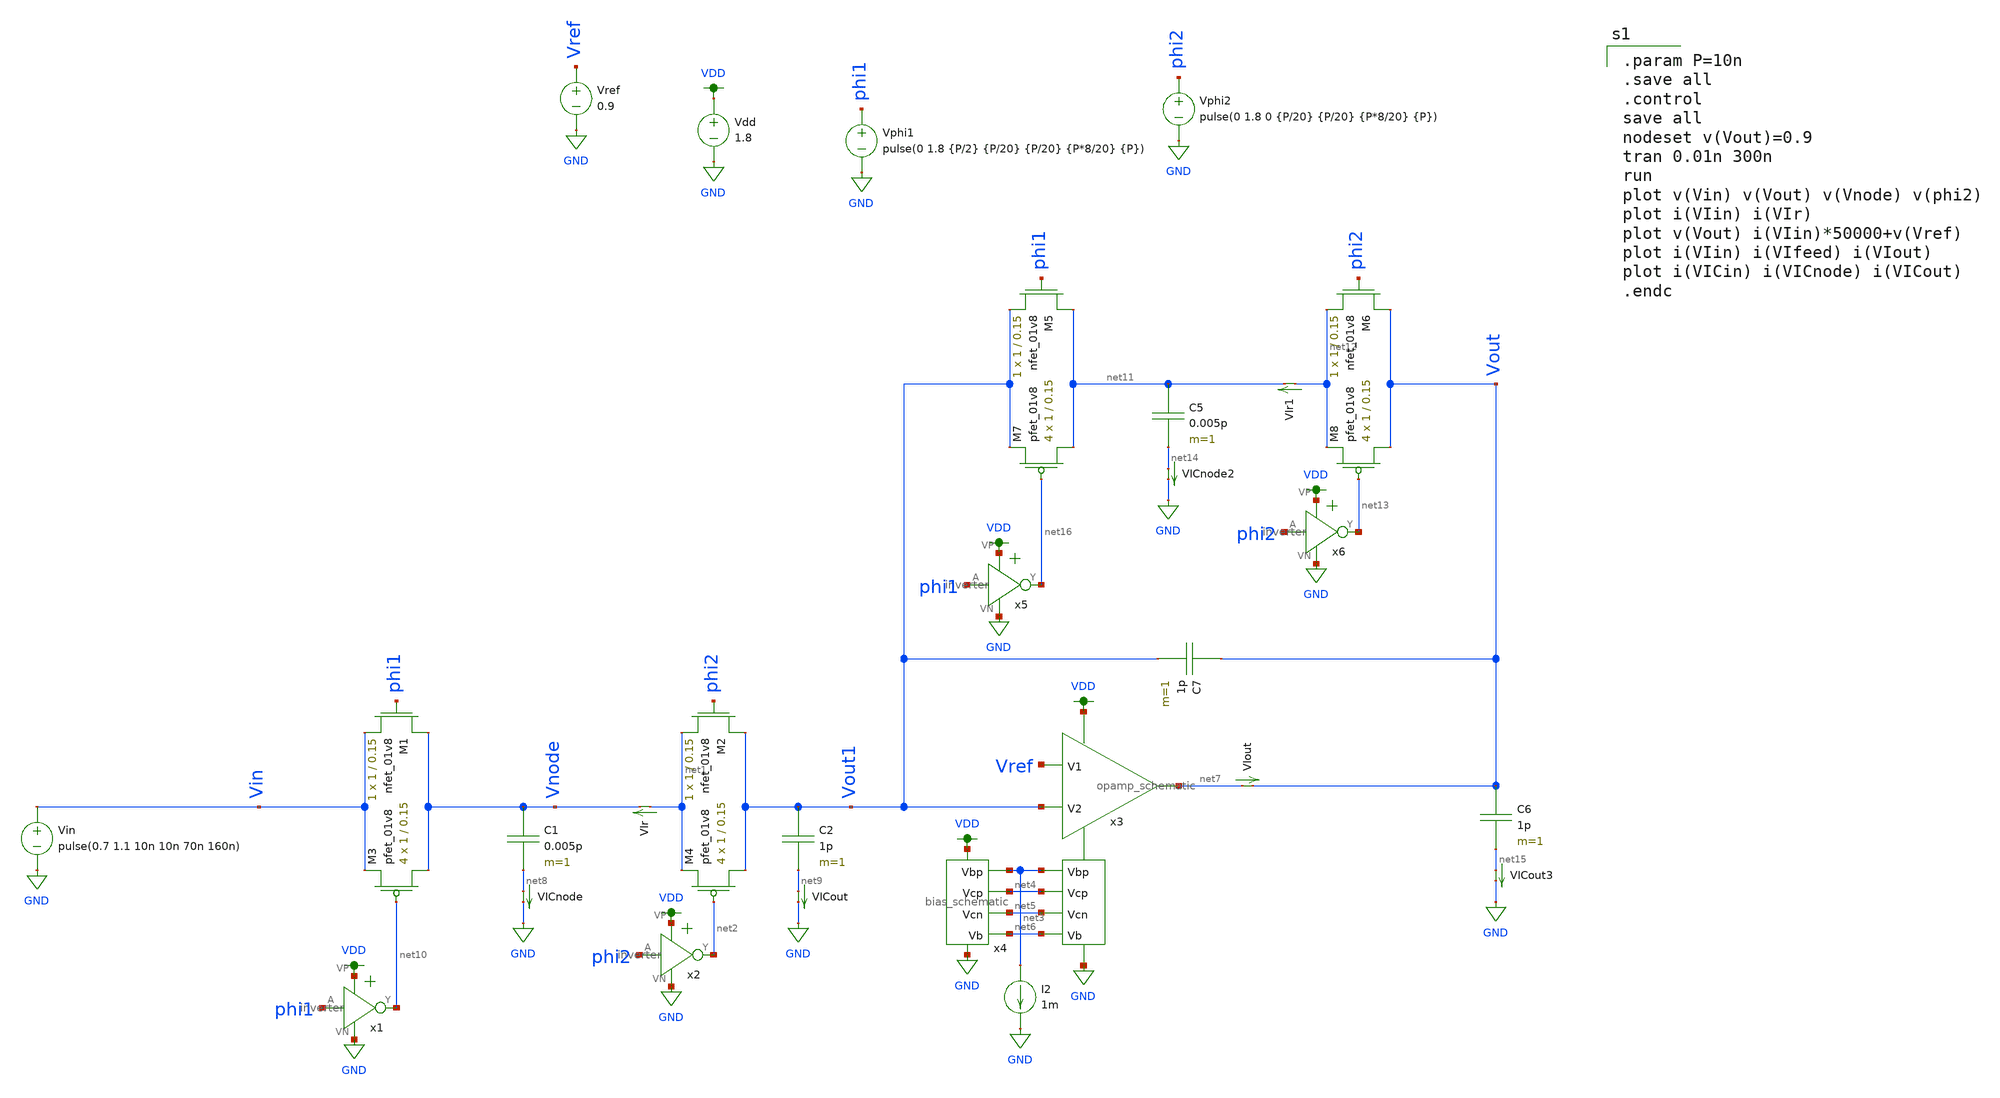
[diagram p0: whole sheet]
** sch_path: xschem/switched_capacitor/switched_capacitor_second_stage_lpf.sch
**.subckt switched_capacitor_second_stage_lpf
C1 Vnode net8 0.005p m=1
XM1 Vnode phi1 Vin GND sky130_fd_pr__nfet_01v8 L=0.15 W=1 nf=1 ad='int((nf+1)/2) * W/nf * 0.29' as='int((nf+2)/2) * W/nf * 0.29'
+ pd='2*int((nf+1)/2) * (W/nf + 0.29)' ps='2*int((nf+2)/2) * (W/nf + 0.29)' nrd='0.29 / W' nrs='0.29 / W'
+ sa=0 sb=0 sd=0 mult=1 m=1
XM2 Vout1 phi2 net1 GND sky130_fd_pr__nfet_01v8 L=0.15 W=1 nf=1 ad='int((nf+1)/2) * W/nf * 0.29' as='int((nf+2)/2) * W/nf * 0.29'
+ pd='2*int((nf+1)/2) * (W/nf + 0.29)' ps='2*int((nf+2)/2) * (W/nf + 0.29)' nrd='0.29 / W' nrs='0.29 / W'
+ sa=0 sb=0 sd=0 mult=1 m=1
Vphi1 phi1 GND pulse(0 1.8 {P/2} {P/20} {P/20} {P*8/20} {P})
Vphi2 phi2 GND pulse(0 1.8 0 {P/20} {P/20} {P*8/20} {P})
Vdd VDD GND 1.8
C2 Vout1 net9 1p m=1
XM3 Vnode net10 Vin VDD sky130_fd_pr__pfet_01v8 L=0.15 W=1 nf=1 ad='int((nf+1)/2) * W/nf * 0.29' as='int((nf+2)/2) * W/nf * 0.29'
+ pd='2*int((nf+1)/2) * (W/nf + 0.29)' ps='2*int((nf+2)/2) * (W/nf + 0.29)' nrd='0.29 / W' nrs='0.29 / W'
+ sa=0 sb=0 sd=0 mult=4 m=4
XM4 Vout1 net2 net1 VDD sky130_fd_pr__pfet_01v8 L=0.15 W=1 nf=1 ad='int((nf+1)/2) * W/nf * 0.29' as='int((nf+2)/2) * W/nf * 0.29'
+ pd='2*int((nf+1)/2) * (W/nf + 0.29)' ps='2*int((nf+2)/2) * (W/nf + 0.29)' nrd='0.29 / W' nrs='0.29 / W'
+ sa=0 sb=0 sd=0 mult=4 m=4
x1 VDD phi1 net10 GND inverter
x2 VDD phi2 net2 GND inverter
x3 VDD net3 net4 net7 Vref Vout1 net5 net6 GND opamp_schematic
x4 VDD net3 net4 net5 GND net6 bias_schematic
Vref Vref GND 0.9
I2 net3 GND 1m
VIr net1 Vnode 0
.save i(vir)
VIout net7 Vout 0
.save i(viout)
VICnode net8 GND 0
.save i(vicnode)
VICout net9 GND 0
.save i(vicout)
C5 net11 net14 0.005p m=1
XM5 net11 phi1 Vout1 GND sky130_fd_pr__nfet_01v8 L=0.15 W=1 nf=1 ad='int((nf+1)/2) * W/nf * 0.29' as='int((nf+2)/2) * W/nf * 0.29'
+ pd='2*int((nf+1)/2) * (W/nf + 0.29)' ps='2*int((nf+2)/2) * (W/nf + 0.29)' nrd='0.29 / W' nrs='0.29 / W'
+ sa=0 sb=0 sd=0 mult=1 m=1
XM6 Vout phi2 net12 GND sky130_fd_pr__nfet_01v8 L=0.15 W=1 nf=1 ad='int((nf+1)/2) * W/nf * 0.29' as='int((nf+2)/2) * W/nf * 0.29'
+ pd='2*int((nf+1)/2) * (W/nf + 0.29)' ps='2*int((nf+2)/2) * (W/nf + 0.29)' nrd='0.29 / W' nrs='0.29 / W'
+ sa=0 sb=0 sd=0 mult=1 m=1
C6 Vout net15 1p m=1
XM7 net11 net16 Vout1 VDD sky130_fd_pr__pfet_01v8 L=0.15 W=1 nf=1 ad='int((nf+1)/2) * W/nf * 0.29' as='int((nf+2)/2) * W/nf * 0.29'
+ pd='2*int((nf+1)/2) * (W/nf + 0.29)' ps='2*int((nf+2)/2) * (W/nf + 0.29)' nrd='0.29 / W' nrs='0.29 / W'
+ sa=0 sb=0 sd=0 mult=4 m=4
XM8 Vout net13 net12 VDD sky130_fd_pr__pfet_01v8 L=0.15 W=1 nf=1 ad='int((nf+1)/2) * W/nf * 0.29' as='int((nf+2)/2) * W/nf * 0.29'
+ pd='2*int((nf+1)/2) * (W/nf + 0.29)' ps='2*int((nf+2)/2) * (W/nf + 0.29)' nrd='0.29 / W' nrs='0.29 / W'
+ sa=0 sb=0 sd=0 mult=4 m=4
x5 VDD phi1 net16 GND inverter
x6 VDD phi2 net13 GND inverter
VIr1 net12 net11 0
.save i(vir1)
VICnode2 net14 GND 0
.save i(vicnode2)
VICout3 net15 GND 0
.save i(vicout3)
C7 Vout Vout1 1p m=1
Vin Vin GND pulse(0.7 1.1 10n 10n 70n 160n)
**** begin user architecture code

.option wnflag=1
.param MC_SWITCH=0.0
.lib ~/skywater/skywater-pdk/libraries/sky130_fd_pr_ngspice/latest/models/sky130.lib.spice tt


.param P=10n
.save all
.control
save all
nodeset v(Vout)=0.9
tran 0.01n 300n
run
plot v(Vin) v(Vout) v(Vnode) v(phi2)
plot i(VIin) i(VIr)
plot v(Vout) i(VIin)*50000+v(Vref)
plot i(VIin) i(VIfeed) i(VIout)
plot i(VICin) i(VICnode) i(VICout)
.endc

**** end user architecture code
**.ends

* expanding   symbol:  /home/madvlsi/dev/git/magic-dds/xschem/other_project_files/inverter.sym # of
*+ pins=4
** sym_path: xschem/other_project_files/inverter.sym
** sch_path: xschem/other_project_files/inverter.sch
.subckt inverter VP A Y VN
*.iopin VP
*.iopin VN
*.ipin A
*.opin Y
XM1 Y A VN VN sky130_fd_pr__nfet_01v8 L=0.15 W=1 nf=1 ad='int((nf+1)/2) * W/nf * 0.29' as='int((nf+2)/2) * W/nf * 0.29'
+ pd='2*int((nf+1)/2) * (W/nf + 0.29)' ps='2*int((nf+2)/2) * (W/nf + 0.29)' nrd='0.29 / W' nrs='0.29 / W'
+ sa=0 sb=0 sd=0 mult=1 m=1
XM2 Y A VP VP sky130_fd_pr__pfet_01v8 L=0.15 W=4 nf=1 ad='int((nf+1)/2) * W/nf * 0.29' as='int((nf+2)/2) * W/nf * 0.29'
+ pd='2*int((nf+1)/2) * (W/nf + 0.29)' ps='2*int((nf+2)/2) * (W/nf + 0.29)' nrd='0.29 / W' nrs='0.29 / W'
+ sa=0 sb=0 sd=0 mult=1 m=1
.ends


* expanding   symbol:
*+  /home/madvlsi/dev/git/magic-dds/xschem/other_project_files/opamp_schematic.sym # of pins=9
** sym_path: xschem/other_project_files/opamp_schematic.sym
** sch_path: xschem/other_project_files/opamp_schematic.sch
.subckt opamp_schematic VP Vbp Vcp Vout V1 V2 Vcn Vb VN
*.ipin Vbp
*.ipin Vcp
*.ipin Vcn
*.ipin V2
*.ipin V1
*.ipin Vb
*.iopin VP
*.iopin VN
*.opin Vout
XM1a M1top V1 Vnode GND sky130_fd_pr__nfet_01v8 L=0.5 W=3 nf=1 ad='int((nf+1)/2) * W/nf * 0.29' as='int((nf+2)/2) * W/nf * 0.29'
+ pd='2*int((nf+1)/2) * (W/nf + 0.29)' ps='2*int((nf+2)/2) * (W/nf + 0.29)' nrd='0.29 / W' nrs='0.29 / W'
+ sa=0 sb=0 sd=0 mult=1 m=1
XM1b M1top V1 Vnode GND sky130_fd_pr__nfet_01v8 L=0.5 W=3 nf=1 ad='int((nf+1)/2) * W/nf * 0.29' as='int((nf+2)/2) * W/nf * 0.29'
+ pd='2*int((nf+1)/2) * (W/nf + 0.29)' ps='2*int((nf+2)/2) * (W/nf + 0.29)' nrd='0.29 / W' nrs='0.29 / W'
+ sa=0 sb=0 sd=0 mult=1 m=1
XM1c M1top V1 Vnode GND sky130_fd_pr__nfet_01v8 L=0.5 W=3 nf=1 ad='int((nf+1)/2) * W/nf * 0.29' as='int((nf+2)/2) * W/nf * 0.29'
+ pd='2*int((nf+1)/2) * (W/nf + 0.29)' ps='2*int((nf+2)/2) * (W/nf + 0.29)' nrd='0.29 / W' nrs='0.29 / W'
+ sa=0 sb=0 sd=0 mult=1 m=1
XM1d M1top V1 Vnode GND sky130_fd_pr__nfet_01v8 L=0.5 W=3 nf=1 ad='int((nf+1)/2) * W/nf * 0.29' as='int((nf+2)/2) * W/nf * 0.29'
+ pd='2*int((nf+1)/2) * (W/nf + 0.29)' ps='2*int((nf+2)/2) * (W/nf + 0.29)' nrd='0.29 / W' nrs='0.29 / W'
+ sa=0 sb=0 sd=0 mult=1 m=1
XM2a M2top V2 Vnode GND sky130_fd_pr__nfet_01v8 L=0.5 W=3 nf=1 ad='int((nf+1)/2) * W/nf * 0.29' as='int((nf+2)/2) * W/nf * 0.29'
+ pd='2*int((nf+1)/2) * (W/nf + 0.29)' ps='2*int((nf+2)/2) * (W/nf + 0.29)' nrd='0.29 / W' nrs='0.29 / W'
+ sa=0 sb=0 sd=0 mult=1 m=1
XM2b M2top V2 Vnode GND sky130_fd_pr__nfet_01v8 L=0.5 W=3 nf=1 ad='int((nf+1)/2) * W/nf * 0.29' as='int((nf+2)/2) * W/nf * 0.29'
+ pd='2*int((nf+1)/2) * (W/nf + 0.29)' ps='2*int((nf+2)/2) * (W/nf + 0.29)' nrd='0.29 / W' nrs='0.29 / W'
+ sa=0 sb=0 sd=0 mult=1 m=1
XM2c M2top V2 Vnode GND sky130_fd_pr__nfet_01v8 L=0.5 W=3 nf=1 ad='int((nf+1)/2) * W/nf * 0.29' as='int((nf+2)/2) * W/nf * 0.29'
+ pd='2*int((nf+1)/2) * (W/nf + 0.29)' ps='2*int((nf+2)/2) * (W/nf + 0.29)' nrd='0.29 / W' nrs='0.29 / W'
+ sa=0 sb=0 sd=0 mult=1 m=1
XM2d M2top V2 Vnode GND sky130_fd_pr__nfet_01v8 L=0.5 W=3 nf=1 ad='int((nf+1)/2) * W/nf * 0.29' as='int((nf+2)/2) * W/nf * 0.29'
+ pd='2*int((nf+1)/2) * (W/nf + 0.29)' ps='2*int((nf+2)/2) * (W/nf + 0.29)' nrd='0.29 / W' nrs='0.29 / W'
+ sa=0 sb=0 sd=0 mult=1 m=1
XMba Vnode Vb VN GND sky130_fd_pr__nfet_01v8 L=0.5 W=1.5 nf=1 ad='int((nf+1)/2) * W/nf * 0.29' as='int((nf+2)/2) * W/nf * 0.29'
+ pd='2*int((nf+1)/2) * (W/nf + 0.29)' ps='2*int((nf+2)/2) * (W/nf + 0.29)' nrd='0.29 / W' nrs='0.29 / W'
+ sa=0 sb=0 sd=0 mult=1 m=1
XMbb Vnode Vb VN GND sky130_fd_pr__nfet_01v8 L=0.5 W=1.5 nf=1 ad='int((nf+1)/2) * W/nf * 0.29' as='int((nf+2)/2) * W/nf * 0.29'
+ pd='2*int((nf+1)/2) * (W/nf + 0.29)' ps='2*int((nf+2)/2) * (W/nf + 0.29)' nrd='0.29 / W' nrs='0.29 / W'
+ sa=0 sb=0 sd=0 mult=1 m=1
XMbc Vnode Vb VN GND sky130_fd_pr__nfet_01v8 L=0.5 W=1.5 nf=1 ad='int((nf+1)/2) * W/nf * 0.29' as='int((nf+2)/2) * W/nf * 0.29'
+ pd='2*int((nf+1)/2) * (W/nf + 0.29)' ps='2*int((nf+2)/2) * (W/nf + 0.29)' nrd='0.29 / W' nrs='0.29 / W'
+ sa=0 sb=0 sd=0 mult=1 m=1
XMbd Vnode Vb VN GND sky130_fd_pr__nfet_01v8 L=0.5 W=1.5 nf=1 ad='int((nf+1)/2) * W/nf * 0.29' as='int((nf+2)/2) * W/nf * 0.29'
+ pd='2*int((nf+1)/2) * (W/nf + 0.29)' ps='2*int((nf+2)/2) * (W/nf + 0.29)' nrd='0.29 / W' nrs='0.29 / W'
+ sa=0 sb=0 sd=0 mult=1 m=1
XMbe Vnode Vb VN GND sky130_fd_pr__nfet_01v8 L=0.5 W=1.5 nf=1 ad='int((nf+1)/2) * W/nf * 0.29' as='int((nf+2)/2) * W/nf * 0.29'
+ pd='2*int((nf+1)/2) * (W/nf + 0.29)' ps='2*int((nf+2)/2) * (W/nf + 0.29)' nrd='0.29 / W' nrs='0.29 / W'
+ sa=0 sb=0 sd=0 mult=1 m=1
XMbf Vnode Vb VN GND sky130_fd_pr__nfet_01v8 L=0.5 W=1.5 nf=1 ad='int((nf+1)/2) * W/nf * 0.29' as='int((nf+2)/2) * W/nf * 0.29'
+ pd='2*int((nf+1)/2) * (W/nf + 0.29)' ps='2*int((nf+2)/2) * (W/nf + 0.29)' nrd='0.29 / W' nrs='0.29 / W'
+ sa=0 sb=0 sd=0 mult=1 m=1
XMbg Vnode Vb VN GND sky130_fd_pr__nfet_01v8 L=0.5 W=1.5 nf=1 ad='int((nf+1)/2) * W/nf * 0.29' as='int((nf+2)/2) * W/nf * 0.29'
+ pd='2*int((nf+1)/2) * (W/nf + 0.29)' ps='2*int((nf+2)/2) * (W/nf + 0.29)' nrd='0.29 / W' nrs='0.29 / W'
+ sa=0 sb=0 sd=0 mult=1 m=1
XMbh Vnode Vb VN GND sky130_fd_pr__nfet_01v8 L=0.5 W=1.5 nf=1 ad='int((nf+1)/2) * W/nf * 0.29' as='int((nf+2)/2) * W/nf * 0.29'
+ pd='2*int((nf+1)/2) * (W/nf + 0.29)' ps='2*int((nf+2)/2) * (W/nf + 0.29)' nrd='0.29 / W' nrs='0.29 / W'
+ sa=0 sb=0 sd=0 mult=1 m=1
XM7a net2 Vcn net1 GND sky130_fd_pr__nfet_01v8 L=0.5 W=3 nf=1 ad='int((nf+1)/2) * W/nf * 0.29' as='int((nf+2)/2) * W/nf * 0.29'
+ pd='2*int((nf+1)/2) * (W/nf + 0.29)' ps='2*int((nf+2)/2) * (W/nf + 0.29)' nrd='0.29 / W' nrs='0.29 / W'
+ sa=0 sb=0 sd=0 mult=1 m=1
XM7b net2 Vcn net1 GND sky130_fd_pr__nfet_01v8 L=0.5 W=3 nf=1 ad='int((nf+1)/2) * W/nf * 0.29' as='int((nf+2)/2) * W/nf * 0.29'
+ pd='2*int((nf+1)/2) * (W/nf + 0.29)' ps='2*int((nf+2)/2) * (W/nf + 0.29)' nrd='0.29 / W' nrs='0.29 / W'
+ sa=0 sb=0 sd=0 mult=1 m=1
XM7c net2 Vcn net1 GND sky130_fd_pr__nfet_01v8 L=0.5 W=3 nf=1 ad='int((nf+1)/2) * W/nf * 0.29' as='int((nf+2)/2) * W/nf * 0.29'
+ pd='2*int((nf+1)/2) * (W/nf + 0.29)' ps='2*int((nf+2)/2) * (W/nf + 0.29)' nrd='0.29 / W' nrs='0.29 / W'
+ sa=0 sb=0 sd=0 mult=1 m=1
XM7d net2 Vcn net1 GND sky130_fd_pr__nfet_01v8 L=0.5 W=3 nf=1 ad='int((nf+1)/2) * W/nf * 0.29' as='int((nf+2)/2) * W/nf * 0.29'
+ pd='2*int((nf+1)/2) * (W/nf + 0.29)' ps='2*int((nf+2)/2) * (W/nf + 0.29)' nrd='0.29 / W' nrs='0.29 / W'
+ sa=0 sb=0 sd=0 mult=1 m=1
XM8a net3 Vcn Vout GND sky130_fd_pr__nfet_01v8 L=0.5 W=3 nf=1 ad='int((nf+1)/2) * W/nf * 0.29' as='int((nf+2)/2) * W/nf * 0.29'
+ pd='2*int((nf+1)/2) * (W/nf + 0.29)' ps='2*int((nf+2)/2) * (W/nf + 0.29)' nrd='0.29 / W' nrs='0.29 / W'
+ sa=0 sb=0 sd=0 mult=1 m=1
XM8b net3 Vcn Vout GND sky130_fd_pr__nfet_01v8 L=0.5 W=3 nf=1 ad='int((nf+1)/2) * W/nf * 0.29' as='int((nf+2)/2) * W/nf * 0.29'
+ pd='2*int((nf+1)/2) * (W/nf + 0.29)' ps='2*int((nf+2)/2) * (W/nf + 0.29)' nrd='0.29 / W' nrs='0.29 / W'
+ sa=0 sb=0 sd=0 mult=1 m=1
XM8c net3 Vcn Vout GND sky130_fd_pr__nfet_01v8 L=0.5 W=3 nf=1 ad='int((nf+1)/2) * W/nf * 0.29' as='int((nf+2)/2) * W/nf * 0.29'
+ pd='2*int((nf+1)/2) * (W/nf + 0.29)' ps='2*int((nf+2)/2) * (W/nf + 0.29)' nrd='0.29 / W' nrs='0.29 / W'
+ sa=0 sb=0 sd=0 mult=1 m=1
XM8d net3 Vcn Vout GND sky130_fd_pr__nfet_01v8 L=0.5 W=3 nf=1 ad='int((nf+1)/2) * W/nf * 0.29' as='int((nf+2)/2) * W/nf * 0.29'
+ pd='2*int((nf+1)/2) * (W/nf + 0.29)' ps='2*int((nf+2)/2) * (W/nf + 0.29)' nrd='0.29 / W' nrs='0.29 / W'
+ sa=0 sb=0 sd=0 mult=1 m=1
XM9a net1 net2 VN GND sky130_fd_pr__nfet_01v8 L=0.5 W=3 nf=1 ad='int((nf+1)/2) * W/nf * 0.29' as='int((nf+2)/2) * W/nf * 0.29'
+ pd='2*int((nf+1)/2) * (W/nf + 0.29)' ps='2*int((nf+2)/2) * (W/nf + 0.29)' nrd='0.29 / W' nrs='0.29 / W'
+ sa=0 sb=0 sd=0 mult=1 m=1
XM9b net1 net2 VN GND sky130_fd_pr__nfet_01v8 L=0.5 W=3 nf=1 ad='int((nf+1)/2) * W/nf * 0.29' as='int((nf+2)/2) * W/nf * 0.29'
+ pd='2*int((nf+1)/2) * (W/nf + 0.29)' ps='2*int((nf+2)/2) * (W/nf + 0.29)' nrd='0.29 / W' nrs='0.29 / W'
+ sa=0 sb=0 sd=0 mult=1 m=1
XM9c net1 net2 VN GND sky130_fd_pr__nfet_01v8 L=0.5 W=3 nf=1 ad='int((nf+1)/2) * W/nf * 0.29' as='int((nf+2)/2) * W/nf * 0.29'
+ pd='2*int((nf+1)/2) * (W/nf + 0.29)' ps='2*int((nf+2)/2) * (W/nf + 0.29)' nrd='0.29 / W' nrs='0.29 / W'
+ sa=0 sb=0 sd=0 mult=1 m=1
XM9d net1 net2 VN GND sky130_fd_pr__nfet_01v8 L=0.5 W=3 nf=1 ad='int((nf+1)/2) * W/nf * 0.29' as='int((nf+2)/2) * W/nf * 0.29'
+ pd='2*int((nf+1)/2) * (W/nf + 0.29)' ps='2*int((nf+2)/2) * (W/nf + 0.29)' nrd='0.29 / W' nrs='0.29 / W'
+ sa=0 sb=0 sd=0 mult=1 m=1
XM10a VN net2 net3 GND sky130_fd_pr__nfet_01v8 L=0.5 W=3 nf=1 ad='int((nf+1)/2) * W/nf * 0.29' as='int((nf+2)/2) * W/nf * 0.29'
+ pd='2*int((nf+1)/2) * (W/nf + 0.29)' ps='2*int((nf+2)/2) * (W/nf + 0.29)' nrd='0.29 / W' nrs='0.29 / W'
+ sa=0 sb=0 sd=0 mult=1 m=1
XM10b VN net2 net3 GND sky130_fd_pr__nfet_01v8 L=0.5 W=3 nf=1 ad='int((nf+1)/2) * W/nf * 0.29' as='int((nf+2)/2) * W/nf * 0.29'
+ pd='2*int((nf+1)/2) * (W/nf + 0.29)' ps='2*int((nf+2)/2) * (W/nf + 0.29)' nrd='0.29 / W' nrs='0.29 / W'
+ sa=0 sb=0 sd=0 mult=1 m=1
XM10c VN net2 net3 GND sky130_fd_pr__nfet_01v8 L=0.5 W=3 nf=1 ad='int((nf+1)/2) * W/nf * 0.29' as='int((nf+2)/2) * W/nf * 0.29'
+ pd='2*int((nf+1)/2) * (W/nf + 0.29)' ps='2*int((nf+2)/2) * (W/nf + 0.29)' nrd='0.29 / W' nrs='0.29 / W'
+ sa=0 sb=0 sd=0 mult=1 m=1
XM1 VN net2 net3 GND sky130_fd_pr__nfet_01v8 L=0.5 W=3 nf=1 ad='int((nf+1)/2) * W/nf * 0.29' as='int((nf+2)/2) * W/nf * 0.29'
+ pd='2*int((nf+1)/2) * (W/nf + 0.29)' ps='2*int((nf+2)/2) * (W/nf + 0.29)' nrd='0.29 / W' nrs='0.29 / W'
+ sa=0 sb=0 sd=0 mult=1 m=1
XM5a net2 Vcp M1top VDD sky130_fd_pr__pfet_01v8 L=0.5 W=3 nf=1 ad='int((nf+1)/2) * W/nf * 0.29' as='int((nf+2)/2) * W/nf * 0.29'
+ pd='2*int((nf+1)/2) * (W/nf + 0.29)' ps='2*int((nf+2)/2) * (W/nf + 0.29)' nrd='0.29 / W' nrs='0.29 / W'
+ sa=0 sb=0 sd=0 mult=1 m=1
XM5b net2 Vcp M1top VDD sky130_fd_pr__pfet_01v8 L=0.5 W=3 nf=1 ad='int((nf+1)/2) * W/nf * 0.29' as='int((nf+2)/2) * W/nf * 0.29'
+ pd='2*int((nf+1)/2) * (W/nf + 0.29)' ps='2*int((nf+2)/2) * (W/nf + 0.29)' nrd='0.29 / W' nrs='0.29 / W'
+ sa=0 sb=0 sd=0 mult=1 m=1
XM5c net2 Vcp M1top VDD sky130_fd_pr__pfet_01v8 L=0.5 W=3 nf=1 ad='int((nf+1)/2) * W/nf * 0.29' as='int((nf+2)/2) * W/nf * 0.29'
+ pd='2*int((nf+1)/2) * (W/nf + 0.29)' ps='2*int((nf+2)/2) * (W/nf + 0.29)' nrd='0.29 / W' nrs='0.29 / W'
+ sa=0 sb=0 sd=0 mult=1 m=1
XM5d net2 Vcp M1top VDD sky130_fd_pr__pfet_01v8 L=0.5 W=3 nf=1 ad='int((nf+1)/2) * W/nf * 0.29' as='int((nf+2)/2) * W/nf * 0.29'
+ pd='2*int((nf+1)/2) * (W/nf + 0.29)' ps='2*int((nf+2)/2) * (W/nf + 0.29)' nrd='0.29 / W' nrs='0.29 / W'
+ sa=0 sb=0 sd=0 mult=1 m=1
XM6a Vout Vcp M2top VDD sky130_fd_pr__pfet_01v8 L=0.5 W=3 nf=1 ad='int((nf+1)/2) * W/nf * 0.29' as='int((nf+2)/2) * W/nf * 0.29'
+ pd='2*int((nf+1)/2) * (W/nf + 0.29)' ps='2*int((nf+2)/2) * (W/nf + 0.29)' nrd='0.29 / W' nrs='0.29 / W'
+ sa=0 sb=0 sd=0 mult=1 m=1
XM6b Vout Vcp M2top VDD sky130_fd_pr__pfet_01v8 L=0.5 W=3 nf=1 ad='int((nf+1)/2) * W/nf * 0.29' as='int((nf+2)/2) * W/nf * 0.29'
+ pd='2*int((nf+1)/2) * (W/nf + 0.29)' ps='2*int((nf+2)/2) * (W/nf + 0.29)' nrd='0.29 / W' nrs='0.29 / W'
+ sa=0 sb=0 sd=0 mult=1 m=1
XM6c Vout Vcp M2top VDD sky130_fd_pr__pfet_01v8 L=0.5 W=3 nf=1 ad='int((nf+1)/2) * W/nf * 0.29' as='int((nf+2)/2) * W/nf * 0.29'
+ pd='2*int((nf+1)/2) * (W/nf + 0.29)' ps='2*int((nf+2)/2) * (W/nf + 0.29)' nrd='0.29 / W' nrs='0.29 / W'
+ sa=0 sb=0 sd=0 mult=1 m=1
XM6d Vout Vcp M2top VDD sky130_fd_pr__pfet_01v8 L=0.5 W=3 nf=1 ad='int((nf+1)/2) * W/nf * 0.29' as='int((nf+2)/2) * W/nf * 0.29'
+ pd='2*int((nf+1)/2) * (W/nf + 0.29)' ps='2*int((nf+2)/2) * (W/nf + 0.29)' nrd='0.29 / W' nrs='0.29 / W'
+ sa=0 sb=0 sd=0 mult=1 m=1
XM3a M1top Vbp VP VDD sky130_fd_pr__pfet_01v8 L=0.5 W=3 nf=1 ad='int((nf+1)/2) * W/nf * 0.29' as='int((nf+2)/2) * W/nf * 0.29'
+ pd='2*int((nf+1)/2) * (W/nf + 0.29)' ps='2*int((nf+2)/2) * (W/nf + 0.29)' nrd='0.29 / W' nrs='0.29 / W'
+ sa=0 sb=0 sd=0 mult=1 m=1
XM3b M1top Vbp VP VDD sky130_fd_pr__pfet_01v8 L=0.5 W=3 nf=1 ad='int((nf+1)/2) * W/nf * 0.29' as='int((nf+2)/2) * W/nf * 0.29'
+ pd='2*int((nf+1)/2) * (W/nf + 0.29)' ps='2*int((nf+2)/2) * (W/nf + 0.29)' nrd='0.29 / W' nrs='0.29 / W'
+ sa=0 sb=0 sd=0 mult=1 m=1
XM3c M1top Vbp VP VDD sky130_fd_pr__pfet_01v8 L=0.5 W=3 nf=1 ad='int((nf+1)/2) * W/nf * 0.29' as='int((nf+2)/2) * W/nf * 0.29'
+ pd='2*int((nf+1)/2) * (W/nf + 0.29)' ps='2*int((nf+2)/2) * (W/nf + 0.29)' nrd='0.29 / W' nrs='0.29 / W'
+ sa=0 sb=0 sd=0 mult=1 m=1
XM3d M1top Vbp VP VDD sky130_fd_pr__pfet_01v8 L=0.5 W=3 nf=1 ad='int((nf+1)/2) * W/nf * 0.29' as='int((nf+2)/2) * W/nf * 0.29'
+ pd='2*int((nf+1)/2) * (W/nf + 0.29)' ps='2*int((nf+2)/2) * (W/nf + 0.29)' nrd='0.29 / W' nrs='0.29 / W'
+ sa=0 sb=0 sd=0 mult=1 m=1
XM4a M2top Vbp VP VDD sky130_fd_pr__pfet_01v8 L=0.5 W=3 nf=1 ad='int((nf+1)/2) * W/nf * 0.29' as='int((nf+2)/2) * W/nf * 0.29'
+ pd='2*int((nf+1)/2) * (W/nf + 0.29)' ps='2*int((nf+2)/2) * (W/nf + 0.29)' nrd='0.29 / W' nrs='0.29 / W'
+ sa=0 sb=0 sd=0 mult=1 m=1
XM4b M2top Vbp VP VDD sky130_fd_pr__pfet_01v8 L=0.5 W=3 nf=1 ad='int((nf+1)/2) * W/nf * 0.29' as='int((nf+2)/2) * W/nf * 0.29'
+ pd='2*int((nf+1)/2) * (W/nf + 0.29)' ps='2*int((nf+2)/2) * (W/nf + 0.29)' nrd='0.29 / W' nrs='0.29 / W'
+ sa=0 sb=0 sd=0 mult=1 m=1
XM4c M2top Vbp VP VDD sky130_fd_pr__pfet_01v8 L=0.5 W=3 nf=1 ad='int((nf+1)/2) * W/nf * 0.29' as='int((nf+2)/2) * W/nf * 0.29'
+ pd='2*int((nf+1)/2) * (W/nf + 0.29)' ps='2*int((nf+2)/2) * (W/nf + 0.29)' nrd='0.29 / W' nrs='0.29 / W'
+ sa=0 sb=0 sd=0 mult=1 m=1
XM4d M2top Vbp VP VDD sky130_fd_pr__pfet_01v8 L=0.5 W=3 nf=1 ad='int((nf+1)/2) * W/nf * 0.29' as='int((nf+2)/2) * W/nf * 0.29'
+ pd='2*int((nf+1)/2) * (W/nf + 0.29)' ps='2*int((nf+2)/2) * (W/nf + 0.29)' nrd='0.29 / W' nrs='0.29 / W'
+ sa=0 sb=0 sd=0 mult=1 m=1
.ends


* expanding   symbol:  /home/madvlsi/dev/git/magic-dds/xschem/other_project_files/bias_schematic.sym
*+ # of pins=6
** sym_path: xschem/other_project_files/bias_schematic.sym
** sch_path: xschem/other_project_files/bias_schematic.sch
.subckt bias_schematic VP Vbp Vcp Vcn VN Vb
*.iopin VP
*.iopin VN
*.opin Vcp
*.iopin Vbp
*.opin Vcn
*.opin Vb
XM1a net2 net2 net1 GND sky130_fd_pr__nfet_01v8 L=0.5 W=3 nf=1 ad='int((nf+1)/2) * W/nf * 0.29' as='int((nf+2)/2) * W/nf * 0.29'
+ pd='2*int((nf+1)/2) * (W/nf + 0.29)' ps='2*int((nf+2)/2) * (W/nf + 0.29)' nrd='0.29 / W' nrs='0.29 / W'
+ sa=0 sb=0 sd=0 mult=1 m=1
XM1b net2 net2 net1 GND sky130_fd_pr__nfet_01v8 L=0.5 W=3 nf=1 ad='int((nf+1)/2) * W/nf * 0.29' as='int((nf+2)/2) * W/nf * 0.29'
+ pd='2*int((nf+1)/2) * (W/nf + 0.29)' ps='2*int((nf+2)/2) * (W/nf + 0.29)' nrd='0.29 / W' nrs='0.29 / W'
+ sa=0 sb=0 sd=0 mult=1 m=1
XM1c net2 net2 net1 GND sky130_fd_pr__nfet_01v8 L=0.5 W=3 nf=1 ad='int((nf+1)/2) * W/nf * 0.29' as='int((nf+2)/2) * W/nf * 0.29'
+ pd='2*int((nf+1)/2) * (W/nf + 0.29)' ps='2*int((nf+2)/2) * (W/nf + 0.29)' nrd='0.29 / W' nrs='0.29 / W'
+ sa=0 sb=0 sd=0 mult=1 m=1
XM1d net2 net2 net1 GND sky130_fd_pr__nfet_01v8 L=0.5 W=3 nf=1 ad='int((nf+1)/2) * W/nf * 0.29' as='int((nf+2)/2) * W/nf * 0.29'
+ pd='2*int((nf+1)/2) * (W/nf + 0.29)' ps='2*int((nf+2)/2) * (W/nf + 0.29)' nrd='0.29 / W' nrs='0.29 / W'
+ sa=0 sb=0 sd=0 mult=1 m=1
XM2a VN net2 net1 GND sky130_fd_pr__nfet_01v8 L=0.5 W=3 nf=1 ad='int((nf+1)/2) * W/nf * 0.29' as='int((nf+2)/2) * W/nf * 0.29'
+ pd='2*int((nf+1)/2) * (W/nf + 0.29)' ps='2*int((nf+2)/2) * (W/nf + 0.29)' nrd='0.29 / W' nrs='0.29 / W'
+ sa=0 sb=0 sd=0 mult=1 m=1
XM2b VN net2 net1 GND sky130_fd_pr__nfet_01v8 L=0.5 W=3 nf=1 ad='int((nf+1)/2) * W/nf * 0.29' as='int((nf+2)/2) * W/nf * 0.29'
+ pd='2*int((nf+1)/2) * (W/nf + 0.29)' ps='2*int((nf+2)/2) * (W/nf + 0.29)' nrd='0.29 / W' nrs='0.29 / W'
+ sa=0 sb=0 sd=0 mult=1 m=1
XM2c VN net2 net1 GND sky130_fd_pr__nfet_01v8 L=0.5 W=3 nf=1 ad='int((nf+1)/2) * W/nf * 0.29' as='int((nf+2)/2) * W/nf * 0.29'
+ pd='2*int((nf+1)/2) * (W/nf + 0.29)' ps='2*int((nf+2)/2) * (W/nf + 0.29)' nrd='0.29 / W' nrs='0.29 / W'
+ sa=0 sb=0 sd=0 mult=1 m=1
XM2d VN net2 net1 GND sky130_fd_pr__nfet_01v8 L=0.5 W=3 nf=1 ad='int((nf+1)/2) * W/nf * 0.29' as='int((nf+2)/2) * W/nf * 0.29'
+ pd='2*int((nf+1)/2) * (W/nf + 0.29)' ps='2*int((nf+2)/2) * (W/nf + 0.29)' nrd='0.29 / W' nrs='0.29 / W'
+ sa=0 sb=0 sd=0 mult=1 m=1
XM3a net2 Vbp net7 VDD sky130_fd_pr__pfet_01v8 L=0.5 W=3 nf=1 ad='int((nf+1)/2) * W/nf * 0.29' as='int((nf+2)/2) * W/nf * 0.29'
+ pd='2*int((nf+1)/2) * (W/nf + 0.29)' ps='2*int((nf+2)/2) * (W/nf + 0.29)' nrd='0.29 / W' nrs='0.29 / W'
+ sa=0 sb=0 sd=0 mult=1 m=1
XM3b net7 Vbp net6 VDD sky130_fd_pr__pfet_01v8 L=0.5 W=3 nf=1 ad='int((nf+1)/2) * W/nf * 0.29' as='int((nf+2)/2) * W/nf * 0.29'
+ pd='2*int((nf+1)/2) * (W/nf + 0.29)' ps='2*int((nf+2)/2) * (W/nf + 0.29)' nrd='0.29 / W' nrs='0.29 / W'
+ sa=0 sb=0 sd=0 mult=1 m=1
XM3c net6 Vbp net5 VDD sky130_fd_pr__pfet_01v8 L=0.5 W=3 nf=1 ad='int((nf+1)/2) * W/nf * 0.29' as='int((nf+2)/2) * W/nf * 0.29'
+ pd='2*int((nf+1)/2) * (W/nf + 0.29)' ps='2*int((nf+2)/2) * (W/nf + 0.29)' nrd='0.29 / W' nrs='0.29 / W'
+ sa=0 sb=0 sd=0 mult=1 m=1
XM3d net5 Vbp VP VDD sky130_fd_pr__pfet_01v8 L=0.5 W=3 nf=1 ad='int((nf+1)/2) * W/nf * 0.29' as='int((nf+2)/2) * W/nf * 0.29'
+ pd='2*int((nf+1)/2) * (W/nf + 0.29)' ps='2*int((nf+2)/2) * (W/nf + 0.29)' nrd='0.29 / W' nrs='0.29 / W'
+ sa=0 sb=0 sd=0 mult=1 m=1
XM4a Vcn Vbp VP VDD sky130_fd_pr__pfet_01v8 L=0.5 W=3 nf=1 ad='int((nf+1)/2) * W/nf * 0.29' as='int((nf+2)/2) * W/nf * 0.29'
+ pd='2*int((nf+1)/2) * (W/nf + 0.29)' ps='2*int((nf+2)/2) * (W/nf + 0.29)' nrd='0.29 / W' nrs='0.29 / W'
+ sa=0 sb=0 sd=0 mult=1 m=1
XM4b Vcn Vbp VP VDD sky130_fd_pr__pfet_01v8 L=0.5 W=3 nf=1 ad='int((nf+1)/2) * W/nf * 0.29' as='int((nf+2)/2) * W/nf * 0.29'
+ pd='2*int((nf+1)/2) * (W/nf + 0.29)' ps='2*int((nf+2)/2) * (W/nf + 0.29)' nrd='0.29 / W' nrs='0.29 / W'
+ sa=0 sb=0 sd=0 mult=1 m=1
XM4c Vcn Vbp VP VDD sky130_fd_pr__pfet_01v8 L=0.5 W=3 nf=1 ad='int((nf+1)/2) * W/nf * 0.29' as='int((nf+2)/2) * W/nf * 0.29'
+ pd='2*int((nf+1)/2) * (W/nf + 0.29)' ps='2*int((nf+2)/2) * (W/nf + 0.29)' nrd='0.29 / W' nrs='0.29 / W'
+ sa=0 sb=0 sd=0 mult=1 m=1
XM4d Vcn Vbp VP VDD sky130_fd_pr__pfet_01v8 L=0.5 W=3 nf=1 ad='int((nf+1)/2) * W/nf * 0.29' as='int((nf+2)/2) * W/nf * 0.29'
+ pd='2*int((nf+1)/2) * (W/nf + 0.29)' ps='2*int((nf+2)/2) * (W/nf + 0.29)' nrd='0.29 / W' nrs='0.29 / W'
+ sa=0 sb=0 sd=0 mult=1 m=1
XM11a VP Vbp Vbp VDD sky130_fd_pr__pfet_01v8 L=0.5 W=3 nf=1 ad='int((nf+1)/2) * W/nf * 0.29' as='int((nf+2)/2) * W/nf * 0.29'
+ pd='2*int((nf+1)/2) * (W/nf + 0.29)' ps='2*int((nf+2)/2) * (W/nf + 0.29)' nrd='0.29 / W' nrs='0.29 / W'
+ sa=0 sb=0 sd=0 mult=1 m=1
XM11b VP Vbp Vbp VDD sky130_fd_pr__pfet_01v8 L=0.5 W=3 nf=1 ad='int((nf+1)/2) * W/nf * 0.29' as='int((nf+2)/2) * W/nf * 0.29'
+ pd='2*int((nf+1)/2) * (W/nf + 0.29)' ps='2*int((nf+2)/2) * (W/nf + 0.29)' nrd='0.29 / W' nrs='0.29 / W'
+ sa=0 sb=0 sd=0 mult=1 m=1
XM11c VP Vbp Vbp VDD sky130_fd_pr__pfet_01v8 L=0.5 W=3 nf=1 ad='int((nf+1)/2) * W/nf * 0.29' as='int((nf+2)/2) * W/nf * 0.29'
+ pd='2*int((nf+1)/2) * (W/nf + 0.29)' ps='2*int((nf+2)/2) * (W/nf + 0.29)' nrd='0.29 / W' nrs='0.29 / W'
+ sa=0 sb=0 sd=0 mult=1 m=1
XM11d VP Vbp Vbp VDD sky130_fd_pr__pfet_01v8 L=0.5 W=3 nf=1 ad='int((nf+1)/2) * W/nf * 0.29' as='int((nf+2)/2) * W/nf * 0.29'
+ pd='2*int((nf+1)/2) * (W/nf + 0.29)' ps='2*int((nf+2)/2) * (W/nf + 0.29)' nrd='0.29 / W' nrs='0.29 / W'
+ sa=0 sb=0 sd=0 mult=1 m=1
XM5a net1 Vcn Vcn GND sky130_fd_pr__nfet_01v8 L=0.5 W=3 nf=1 ad='int((nf+1)/2) * W/nf * 0.29' as='int((nf+2)/2) * W/nf * 0.29'
+ pd='2*int((nf+1)/2) * (W/nf + 0.29)' ps='2*int((nf+2)/2) * (W/nf + 0.29)' nrd='0.29 / W' nrs='0.29 / W'
+ sa=0 sb=0 sd=0 mult=1 m=1
XM5b net1 Vcn Vcn GND sky130_fd_pr__nfet_01v8 L=0.5 W=3 nf=1 ad='int((nf+1)/2) * W/nf * 0.29' as='int((nf+2)/2) * W/nf * 0.29'
+ pd='2*int((nf+1)/2) * (W/nf + 0.29)' ps='2*int((nf+2)/2) * (W/nf + 0.29)' nrd='0.29 / W' nrs='0.29 / W'
+ sa=0 sb=0 sd=0 mult=1 m=1
XM5c net1 Vcn Vcn GND sky130_fd_pr__nfet_01v8 L=0.5 W=3 nf=1 ad='int((nf+1)/2) * W/nf * 0.29' as='int((nf+2)/2) * W/nf * 0.29'
+ pd='2*int((nf+1)/2) * (W/nf + 0.29)' ps='2*int((nf+2)/2) * (W/nf + 0.29)' nrd='0.29 / W' nrs='0.29 / W'
+ sa=0 sb=0 sd=0 mult=1 m=1
XM5d net1 Vcn Vcn GND sky130_fd_pr__nfet_01v8 L=0.5 W=3 nf=1 ad='int((nf+1)/2) * W/nf * 0.29' as='int((nf+2)/2) * W/nf * 0.29'
+ pd='2*int((nf+1)/2) * (W/nf + 0.29)' ps='2*int((nf+2)/2) * (W/nf + 0.29)' nrd='0.29 / W' nrs='0.29 / W'
+ sa=0 sb=0 sd=0 mult=1 m=1
XM8a net10 Vb net3 GND sky130_fd_pr__nfet_01v8 L=0.5 W=3 nf=1 ad='int((nf+1)/2) * W/nf * 0.29' as='int((nf+2)/2) * W/nf * 0.29'
+ pd='2*int((nf+1)/2) * (W/nf + 0.29)' ps='2*int((nf+2)/2) * (W/nf + 0.29)' nrd='0.29 / W' nrs='0.29 / W'
+ sa=0 sb=0 sd=0 mult=1 m=1
XM8b net9 Vb net10 GND sky130_fd_pr__nfet_01v8 L=0.5 W=3 nf=1 ad='int((nf+1)/2) * W/nf * 0.29' as='int((nf+2)/2) * W/nf * 0.29'
+ pd='2*int((nf+1)/2) * (W/nf + 0.29)' ps='2*int((nf+2)/2) * (W/nf + 0.29)' nrd='0.29 / W' nrs='0.29 / W'
+ sa=0 sb=0 sd=0 mult=1 m=1
XM8c net8 Vb net9 GND sky130_fd_pr__nfet_01v8 L=0.5 W=3 nf=1 ad='int((nf+1)/2) * W/nf * 0.29' as='int((nf+2)/2) * W/nf * 0.29'
+ pd='2*int((nf+1)/2) * (W/nf + 0.29)' ps='2*int((nf+2)/2) * (W/nf + 0.29)' nrd='0.29 / W' nrs='0.29 / W'
+ sa=0 sb=0 sd=0 mult=1 m=1
XM8d VN Vb net8 GND sky130_fd_pr__nfet_01v8 L=0.5 W=3 nf=1 ad='int((nf+1)/2) * W/nf * 0.29' as='int((nf+2)/2) * W/nf * 0.29'
+ pd='2*int((nf+1)/2) * (W/nf + 0.29)' ps='2*int((nf+2)/2) * (W/nf + 0.29)' nrd='0.29 / W' nrs='0.29 / W'
+ sa=0 sb=0 sd=0 mult=1 m=1
XM6a net3 net3 net4 VDD sky130_fd_pr__pfet_01v8 L=0.5 W=3 nf=1 ad='int((nf+1)/2) * W/nf * 0.29' as='int((nf+2)/2) * W/nf * 0.29'
+ pd='2*int((nf+1)/2) * (W/nf + 0.29)' ps='2*int((nf+2)/2) * (W/nf + 0.29)' nrd='0.29 / W' nrs='0.29 / W'
+ sa=0 sb=0 sd=0 mult=1 m=1
XM6b net3 net3 net4 VDD sky130_fd_pr__pfet_01v8 L=0.5 W=3 nf=1 ad='int((nf+1)/2) * W/nf * 0.29' as='int((nf+2)/2) * W/nf * 0.29'
+ pd='2*int((nf+1)/2) * (W/nf + 0.29)' ps='2*int((nf+2)/2) * (W/nf + 0.29)' nrd='0.29 / W' nrs='0.29 / W'
+ sa=0 sb=0 sd=0 mult=1 m=1
XM6c net3 net3 net4 VDD sky130_fd_pr__pfet_01v8 L=0.5 W=3 nf=1 ad='int((nf+1)/2) * W/nf * 0.29' as='int((nf+2)/2) * W/nf * 0.29'
+ pd='2*int((nf+1)/2) * (W/nf + 0.29)' ps='2*int((nf+2)/2) * (W/nf + 0.29)' nrd='0.29 / W' nrs='0.29 / W'
+ sa=0 sb=0 sd=0 mult=1 m=1
XM6d net3 net3 net4 VDD sky130_fd_pr__pfet_01v8 L=0.5 W=3 nf=1 ad='int((nf+1)/2) * W/nf * 0.29' as='int((nf+2)/2) * W/nf * 0.29'
+ pd='2*int((nf+1)/2) * (W/nf + 0.29)' ps='2*int((nf+2)/2) * (W/nf + 0.29)' nrd='0.29 / W' nrs='0.29 / W'
+ sa=0 sb=0 sd=0 mult=1 m=1
XM7a net4 net3 VP VDD sky130_fd_pr__pfet_01v8 L=0.5 W=3 nf=1 ad='int((nf+1)/2) * W/nf * 0.29' as='int((nf+2)/2) * W/nf * 0.29'
+ pd='2*int((nf+1)/2) * (W/nf + 0.29)' ps='2*int((nf+2)/2) * (W/nf + 0.29)' nrd='0.29 / W' nrs='0.29 / W'
+ sa=0 sb=0 sd=0 mult=1 m=1
XM7b net4 net3 VP VDD sky130_fd_pr__pfet_01v8 L=0.5 W=3 nf=1 ad='int((nf+1)/2) * W/nf * 0.29' as='int((nf+2)/2) * W/nf * 0.29'
+ pd='2*int((nf+1)/2) * (W/nf + 0.29)' ps='2*int((nf+2)/2) * (W/nf + 0.29)' nrd='0.29 / W' nrs='0.29 / W'
+ sa=0 sb=0 sd=0 mult=1 m=1
XM7c net4 net3 VP VDD sky130_fd_pr__pfet_01v8 L=0.5 W=3 nf=1 ad='int((nf+1)/2) * W/nf * 0.29' as='int((nf+2)/2) * W/nf * 0.29'
+ pd='2*int((nf+1)/2) * (W/nf + 0.29)' ps='2*int((nf+2)/2) * (W/nf + 0.29)' nrd='0.29 / W' nrs='0.29 / W'
+ sa=0 sb=0 sd=0 mult=1 m=1
XM7d net4 net3 VP VDD sky130_fd_pr__pfet_01v8 L=0.5 W=3 nf=1 ad='int((nf+1)/2) * W/nf * 0.29' as='int((nf+2)/2) * W/nf * 0.29'
+ pd='2*int((nf+1)/2) * (W/nf + 0.29)' ps='2*int((nf+2)/2) * (W/nf + 0.29)' nrd='0.29 / W' nrs='0.29 / W'
+ sa=0 sb=0 sd=0 mult=1 m=1
XM10d net4 Vcp Vcp VDD sky130_fd_pr__pfet_01v8 L=0.5 W=3 nf=1 ad='int((nf+1)/2) * W/nf * 0.29' as='int((nf+2)/2) * W/nf * 0.29'
+ pd='2*int((nf+1)/2) * (W/nf + 0.29)' ps='2*int((nf+2)/2) * (W/nf + 0.29)' nrd='0.29 / W' nrs='0.29 / W'
+ sa=0 sb=0 sd=0 mult=1 m=1
XM10c net4 Vcp Vcp VDD sky130_fd_pr__pfet_01v8 L=0.5 W=3 nf=1 ad='int((nf+1)/2) * W/nf * 0.29' as='int((nf+2)/2) * W/nf * 0.29'
+ pd='2*int((nf+1)/2) * (W/nf + 0.29)' ps='2*int((nf+2)/2) * (W/nf + 0.29)' nrd='0.29 / W' nrs='0.29 / W'
+ sa=0 sb=0 sd=0 mult=1 m=1
XM10b net4 Vcp Vcp VDD sky130_fd_pr__pfet_01v8 L=0.5 W=3 nf=1 ad='int((nf+1)/2) * W/nf * 0.29' as='int((nf+2)/2) * W/nf * 0.29'
+ pd='2*int((nf+1)/2) * (W/nf + 0.29)' ps='2*int((nf+2)/2) * (W/nf + 0.29)' nrd='0.29 / W' nrs='0.29 / W'
+ sa=0 sb=0 sd=0 mult=1 m=1
XM10a net4 Vcp Vcp VDD sky130_fd_pr__pfet_01v8 L=0.5 W=3 nf=1 ad='int((nf+1)/2) * W/nf * 0.29' as='int((nf+2)/2) * W/nf * 0.29'
+ pd='2*int((nf+1)/2) * (W/nf + 0.29)' ps='2*int((nf+2)/2) * (W/nf + 0.29)' nrd='0.29 / W' nrs='0.29 / W'
+ sa=0 sb=0 sd=0 mult=1 m=1
XM9a VN Vb Vcp GND sky130_fd_pr__nfet_01v8 L=0.5 W=3 nf=1 ad='int((nf+1)/2) * W/nf * 0.29' as='int((nf+2)/2) * W/nf * 0.29'
+ pd='2*int((nf+1)/2) * (W/nf + 0.29)' ps='2*int((nf+2)/2) * (W/nf + 0.29)' nrd='0.29 / W' nrs='0.29 / W'
+ sa=0 sb=0 sd=0 mult=1 m=1
XM9b VN Vb Vcp GND sky130_fd_pr__nfet_01v8 L=0.5 W=3 nf=1 ad='int((nf+1)/2) * W/nf * 0.29' as='int((nf+2)/2) * W/nf * 0.29'
+ pd='2*int((nf+1)/2) * (W/nf + 0.29)' ps='2*int((nf+2)/2) * (W/nf + 0.29)' nrd='0.29 / W' nrs='0.29 / W'
+ sa=0 sb=0 sd=0 mult=1 m=1
XM9c VN Vb Vcp GND sky130_fd_pr__nfet_01v8 L=0.5 W=3 nf=1 ad='int((nf+1)/2) * W/nf * 0.29' as='int((nf+2)/2) * W/nf * 0.29'
+ pd='2*int((nf+1)/2) * (W/nf + 0.29)' ps='2*int((nf+2)/2) * (W/nf + 0.29)' nrd='0.29 / W' nrs='0.29 / W'
+ sa=0 sb=0 sd=0 mult=1 m=1
XM9d VN Vb Vcp GND sky130_fd_pr__nfet_01v8 L=0.5 W=3 nf=1 ad='int((nf+1)/2) * W/nf * 0.29' as='int((nf+2)/2) * W/nf * 0.29'
+ pd='2*int((nf+1)/2) * (W/nf + 0.29)' ps='2*int((nf+2)/2) * (W/nf + 0.29)' nrd='0.29 / W' nrs='0.29 / W'
+ sa=0 sb=0 sd=0 mult=1 m=1
XM12a VN Vb Vb GND sky130_fd_pr__nfet_01v8 L=0.5 W=3 nf=1 ad='int((nf+1)/2) * W/nf * 0.29' as='int((nf+2)/2) * W/nf * 0.29'
+ pd='2*int((nf+1)/2) * (W/nf + 0.29)' ps='2*int((nf+2)/2) * (W/nf + 0.29)' nrd='0.29 / W' nrs='0.29 / W'
+ sa=0 sb=0 sd=0 mult=1 m=1
XM12b VN Vb Vb GND sky130_fd_pr__nfet_01v8 L=0.5 W=3 nf=1 ad='int((nf+1)/2) * W/nf * 0.29' as='int((nf+2)/2) * W/nf * 0.29'
+ pd='2*int((nf+1)/2) * (W/nf + 0.29)' ps='2*int((nf+2)/2) * (W/nf + 0.29)' nrd='0.29 / W' nrs='0.29 / W'
+ sa=0 sb=0 sd=0 mult=1 m=1
XM12c VN Vb Vb GND sky130_fd_pr__nfet_01v8 L=0.5 W=3 nf=1 ad='int((nf+1)/2) * W/nf * 0.29' as='int((nf+2)/2) * W/nf * 0.29'
+ pd='2*int((nf+1)/2) * (W/nf + 0.29)' ps='2*int((nf+2)/2) * (W/nf + 0.29)' nrd='0.29 / W' nrs='0.29 / W'
+ sa=0 sb=0 sd=0 mult=1 m=1
XM12d VN Vb Vb GND sky130_fd_pr__nfet_01v8 L=0.5 W=3 nf=1 ad='int((nf+1)/2) * W/nf * 0.29' as='int((nf+2)/2) * W/nf * 0.29'
+ pd='2*int((nf+1)/2) * (W/nf + 0.29)' ps='2*int((nf+2)/2) * (W/nf + 0.29)' nrd='0.29 / W' nrs='0.29 / W'
+ sa=0 sb=0 sd=0 mult=1 m=1
XM1 Vb Vbp VP VDD sky130_fd_pr__pfet_01v8 L=0.5 W=3 nf=1 ad='int((nf+1)/2) * W/nf * 0.29' as='int((nf+2)/2) * W/nf * 0.29'
+ pd='2*int((nf+1)/2) * (W/nf + 0.29)' ps='2*int((nf+2)/2) * (W/nf + 0.29)' nrd='0.29 / W' nrs='0.29 / W'
+ sa=0 sb=0 sd=0 mult=1 m=1
XM2 Vb Vbp VP VDD sky130_fd_pr__pfet_01v8 L=0.5 W=3 nf=1 ad='int((nf+1)/2) * W/nf * 0.29' as='int((nf+2)/2) * W/nf * 0.29'
+ pd='2*int((nf+1)/2) * (W/nf + 0.29)' ps='2*int((nf+2)/2) * (W/nf + 0.29)' nrd='0.29 / W' nrs='0.29 / W'
+ sa=0 sb=0 sd=0 mult=1 m=1
XM3 Vb Vbp VP VDD sky130_fd_pr__pfet_01v8 L=0.5 W=3 nf=1 ad='int((nf+1)/2) * W/nf * 0.29' as='int((nf+2)/2) * W/nf * 0.29'
+ pd='2*int((nf+1)/2) * (W/nf + 0.29)' ps='2*int((nf+2)/2) * (W/nf + 0.29)' nrd='0.29 / W' nrs='0.29 / W'
+ sa=0 sb=0 sd=0 mult=1 m=1
XM4 Vb Vbp VP VDD sky130_fd_pr__pfet_01v8 L=0.5 W=3 nf=1 ad='int((nf+1)/2) * W/nf * 0.29' as='int((nf+2)/2) * W/nf * 0.29'
+ pd='2*int((nf+1)/2) * (W/nf + 0.29)' ps='2*int((nf+2)/2) * (W/nf + 0.29)' nrd='0.29 / W' nrs='0.29 / W'
+ sa=0 sb=0 sd=0 mult=1 m=1
XM1e net2 net2 net1 GND sky130_fd_pr__nfet_01v8 L=0.5 W=3 nf=1 ad='int((nf+1)/2) * W/nf * 0.29' as='int((nf+2)/2) * W/nf * 0.29'
+ pd='2*int((nf+1)/2) * (W/nf + 0.29)' ps='2*int((nf+2)/2) * (W/nf + 0.29)' nrd='0.29 / W' nrs='0.29 / W'
+ sa=0 sb=0 sd=0 mult=1 m=1
XM1f net2 net2 net1 GND sky130_fd_pr__nfet_01v8 L=0.5 W=3 nf=1 ad='int((nf+1)/2) * W/nf * 0.29' as='int((nf+2)/2) * W/nf * 0.29'
+ pd='2*int((nf+1)/2) * (W/nf + 0.29)' ps='2*int((nf+2)/2) * (W/nf + 0.29)' nrd='0.29 / W' nrs='0.29 / W'
+ sa=0 sb=0 sd=0 mult=1 m=1
XM1g net2 net2 net1 GND sky130_fd_pr__nfet_01v8 L=0.5 W=3 nf=1 ad='int((nf+1)/2) * W/nf * 0.29' as='int((nf+2)/2) * W/nf * 0.29'
+ pd='2*int((nf+1)/2) * (W/nf + 0.29)' ps='2*int((nf+2)/2) * (W/nf + 0.29)' nrd='0.29 / W' nrs='0.29 / W'
+ sa=0 sb=0 sd=0 mult=1 m=1
XM1h net2 net2 net1 GND sky130_fd_pr__nfet_01v8 L=0.5 W=3 nf=1 ad='int((nf+1)/2) * W/nf * 0.29' as='int((nf+2)/2) * W/nf * 0.29'
+ pd='2*int((nf+1)/2) * (W/nf + 0.29)' ps='2*int((nf+2)/2) * (W/nf + 0.29)' nrd='0.29 / W' nrs='0.29 / W'
+ sa=0 sb=0 sd=0 mult=1 m=1
XM6e net3 net3 net4 VDD sky130_fd_pr__pfet_01v8 L=0.5 W=3 nf=1 ad='int((nf+1)/2) * W/nf * 0.29' as='int((nf+2)/2) * W/nf * 0.29'
+ pd='2*int((nf+1)/2) * (W/nf + 0.29)' ps='2*int((nf+2)/2) * (W/nf + 0.29)' nrd='0.29 / W' nrs='0.29 / W'
+ sa=0 sb=0 sd=0 mult=1 m=1
XM6f net3 net3 net4 VDD sky130_fd_pr__pfet_01v8 L=0.5 W=3 nf=1 ad='int((nf+1)/2) * W/nf * 0.29' as='int((nf+2)/2) * W/nf * 0.29'
+ pd='2*int((nf+1)/2) * (W/nf + 0.29)' ps='2*int((nf+2)/2) * (W/nf + 0.29)' nrd='0.29 / W' nrs='0.29 / W'
+ sa=0 sb=0 sd=0 mult=1 m=1
XM6g net3 net3 net4 VDD sky130_fd_pr__pfet_01v8 L=0.5 W=3 nf=1 ad='int((nf+1)/2) * W/nf * 0.29' as='int((nf+2)/2) * W/nf * 0.29'
+ pd='2*int((nf+1)/2) * (W/nf + 0.29)' ps='2*int((nf+2)/2) * (W/nf + 0.29)' nrd='0.29 / W' nrs='0.29 / W'
+ sa=0 sb=0 sd=0 mult=1 m=1
XM6h net3 net3 net4 VDD sky130_fd_pr__pfet_01v8 L=0.5 W=3 nf=1 ad='int((nf+1)/2) * W/nf * 0.29' as='int((nf+2)/2) * W/nf * 0.29'
+ pd='2*int((nf+1)/2) * (W/nf + 0.29)' ps='2*int((nf+2)/2) * (W/nf + 0.29)' nrd='0.29 / W' nrs='0.29 / W'
+ sa=0 sb=0 sd=0 mult=1 m=1
XM1i net2 net2 net1 GND sky130_fd_pr__nfet_01v8 L=0.5 W=3 nf=1 ad='int((nf+1)/2) * W/nf * 0.29' as='int((nf+2)/2) * W/nf * 0.29'
+ pd='2*int((nf+1)/2) * (W/nf + 0.29)' ps='2*int((nf+2)/2) * (W/nf + 0.29)' nrd='0.29 / W' nrs='0.29 / W'
+ sa=0 sb=0 sd=0 mult=1 m=1
XM1j net2 net2 net1 GND sky130_fd_pr__nfet_01v8 L=0.5 W=3 nf=1 ad='int((nf+1)/2) * W/nf * 0.29' as='int((nf+2)/2) * W/nf * 0.29'
+ pd='2*int((nf+1)/2) * (W/nf + 0.29)' ps='2*int((nf+2)/2) * (W/nf + 0.29)' nrd='0.29 / W' nrs='0.29 / W'
+ sa=0 sb=0 sd=0 mult=1 m=1
XM1k net2 net2 net1 GND sky130_fd_pr__nfet_01v8 L=0.5 W=3 nf=1 ad='int((nf+1)/2) * W/nf * 0.29' as='int((nf+2)/2) * W/nf * 0.29'
+ pd='2*int((nf+1)/2) * (W/nf + 0.29)' ps='2*int((nf+2)/2) * (W/nf + 0.29)' nrd='0.29 / W' nrs='0.29 / W'
+ sa=0 sb=0 sd=0 mult=1 m=1
XM1l net2 net2 net1 GND sky130_fd_pr__nfet_01v8 L=0.5 W=3 nf=1 ad='int((nf+1)/2) * W/nf * 0.29' as='int((nf+2)/2) * W/nf * 0.29'
+ pd='2*int((nf+1)/2) * (W/nf + 0.29)' ps='2*int((nf+2)/2) * (W/nf + 0.29)' nrd='0.29 / W' nrs='0.29 / W'
+ sa=0 sb=0 sd=0 mult=1 m=1
XM6i net3 net3 net4 VDD sky130_fd_pr__pfet_01v8 L=0.5 W=3 nf=1 ad='int((nf+1)/2) * W/nf * 0.29' as='int((nf+2)/2) * W/nf * 0.29'
+ pd='2*int((nf+1)/2) * (W/nf + 0.29)' ps='2*int((nf+2)/2) * (W/nf + 0.29)' nrd='0.29 / W' nrs='0.29 / W'
+ sa=0 sb=0 sd=0 mult=1 m=1
XM6j net3 net3 net4 VDD sky130_fd_pr__pfet_01v8 L=0.5 W=3 nf=1 ad='int((nf+1)/2) * W/nf * 0.29' as='int((nf+2)/2) * W/nf * 0.29'
+ pd='2*int((nf+1)/2) * (W/nf + 0.29)' ps='2*int((nf+2)/2) * (W/nf + 0.29)' nrd='0.29 / W' nrs='0.29 / W'
+ sa=0 sb=0 sd=0 mult=1 m=1
XM6k net3 net3 net4 VDD sky130_fd_pr__pfet_01v8 L=0.5 W=3 nf=1 ad='int((nf+1)/2) * W/nf * 0.29' as='int((nf+2)/2) * W/nf * 0.29'
+ pd='2*int((nf+1)/2) * (W/nf + 0.29)' ps='2*int((nf+2)/2) * (W/nf + 0.29)' nrd='0.29 / W' nrs='0.29 / W'
+ sa=0 sb=0 sd=0 mult=1 m=1
XM6l net3 net3 net4 VDD sky130_fd_pr__pfet_01v8 L=0.5 W=3 nf=1 ad='int((nf+1)/2) * W/nf * 0.29' as='int((nf+2)/2) * W/nf * 0.29'
+ pd='2*int((nf+1)/2) * (W/nf + 0.29)' ps='2*int((nf+2)/2) * (W/nf + 0.29)' nrd='0.29 / W' nrs='0.29 / W'
+ sa=0 sb=0 sd=0 mult=1 m=1
.ends

.GLOBAL VDD
.GLOBAL GND
.end
